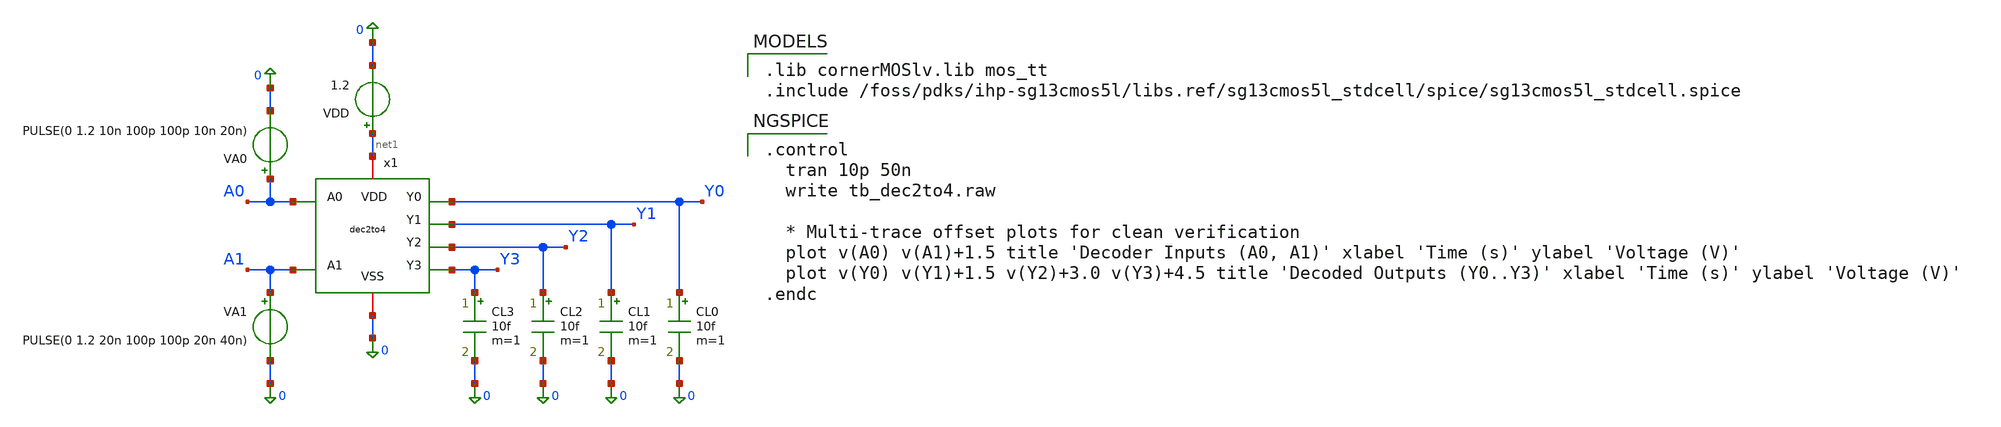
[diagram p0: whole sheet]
** sch_path: designs/libs/core_digital/dec2to4/tb_dec2to4.sch
**.subckt tb_dec2to4
CL3 Y3 0 10f m=1
CL2 Y2 0 10f m=1
CL1 Y1 0 10f m=1
CL0 Y0 0 10f m=1
VDD net1 0 1.2
VA1 A1 0 PULSE(0 1.2 20n 100p 100p 20n 40n)
VA0 A0 0 PULSE(0 1.2 10n 100p 100p 10n 20n)
x1 A0 A1 Y0 Y1 Y2 Y3 net1 0 dec2to4
**** begin user architecture code

.lib cornerMOSlv.lib mos_tt
.include /foss/pdks/ihp-sg13cmos5l/libs.ref/sg13cmos5l_stdcell/spice/sg13cmos5l_stdcell.spice


.control
  tran 10p 50n
  write tb_dec2to4.raw

  * Multi-trace offset plots for clean verification
  plot v(A0) v(A1)+1.5 title 'Decoder Inputs (A0, A1)' xlabel 'Time (s)' ylabel 'Voltage (V)'
  plot v(Y0) v(Y1)+1.5 v(Y2)+3.0 v(Y3)+4.5 title 'Decoded Outputs (Y0..Y3)' xlabel 'Time (s)' ylabel
+ 'Voltage (V)'
.endc

**** end user architecture code
**.ends

* expanding   symbol:  dec2to4.sym # of pins=8
** sym_path: dec2to4.sym
** sch_path: dec2to4.sch
.subckt dec2to4 A0 A1 Y0 Y1 Y2 Y3 VDD VSS
*.ipin A0
*.ipin A1
*.opin Y0
*.opin Y1
*.opin Y2
*.opin Y3
*.iopin VDD
*.iopin VSS
x1 net2 A0 VDD VSS sg13cmos5l_inv_1
x2 net1 A1 VDD VSS sg13cmos5l_inv_1
x11 Y0 net2 net1 VDD VSS sg13cmos5l_and2_1
x3 Y1 A0 net1 VDD VSS sg13cmos5l_and2_1
x4 Y2 A1 net2 VDD VSS sg13cmos5l_and2_1
x5 Y3 A1 A0 VDD VSS sg13cmos5l_and2_1
.ends

.end
